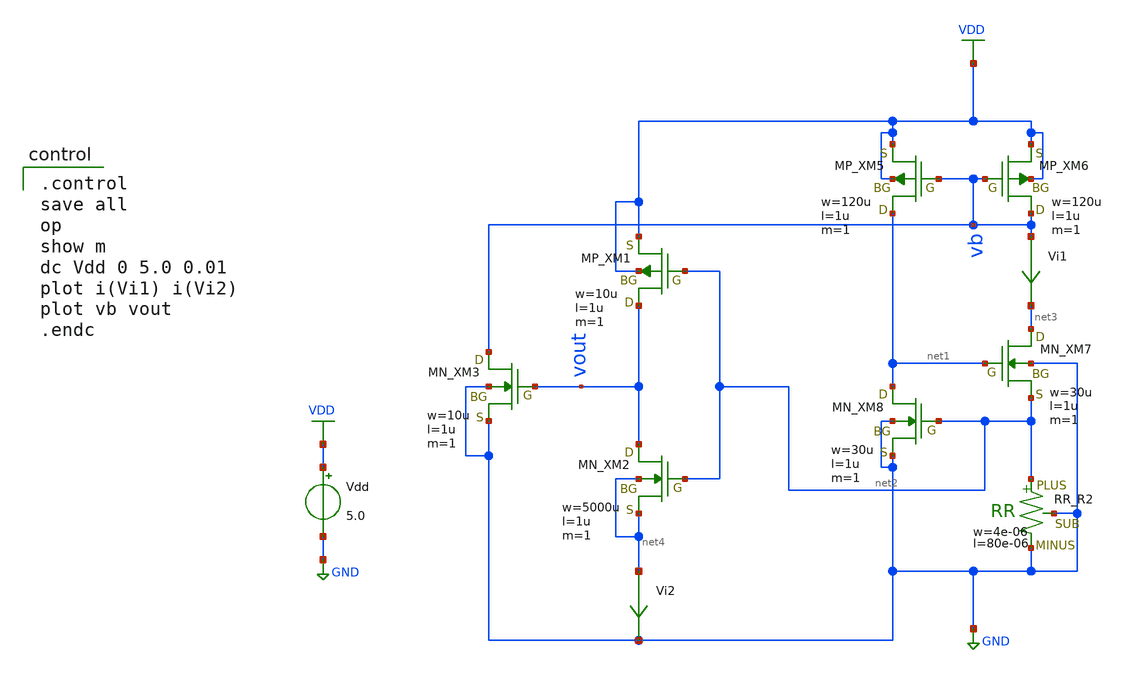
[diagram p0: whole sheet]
** sch_path: schematic/20250924_OSS_Workshop/ishikai/CS/cs_startup_usage_tb.sch
**.subckt cs_startup_usage_tb
Vdd VDD GND 5.0
Vi1 vb net3 0
.save i(vi1)
XM5 net1 vb VDD VDD PMOS w=120u l=1u as=0 ad=0 ps=0 pd=0 nrd=0 nrs=0 m=1
XM6 vb vb VDD VDD PMOS w=120u l=1u as=0 ad=0 ps=0 pd=0 nrd=0 nrs=0 m=1
XM7 net3 net1 net2 GND NMOS w=30u l=1u as=0 ad=0 ps=0 pd=0 nrd=0 nrs=0 m=1
XM8 net1 net2 GND GND NMOS w=30u l=1u as=0 ad=0 ps=0 pd=0 nrd=0 nrs=0 m=1
XR2 net2 GND GND F_RR w=4e-06 R=1 l=80e-06 tc1=0 tc2=0
XM1 vout net2 VDD VDD PMOS w=10u l=1u as=0 ad=0 ps=0 pd=0 nrd=0 nrs=0 m=1
XM2 vout net2 net4 net4 NMOS w=5000u l=1u as=0 ad=0 ps=0 pd=0 nrd=0 nrs=0 m=1
XM3 vb vout GND GND NMOS w=10u l=1u as=0 ad=0 ps=0 pd=0 nrd=0 nrs=0 m=1
Vi2 net4 GND 0
.save i(vi2)
**** begin user architecture code

.control
save all
op
show m
dc Vdd 0 5.0 0.01
plot i(Vi1) i(Vi2)
plot vb vout
.endc

 .include $::LIB/../ip62_models
**** end user architecture code
**.ends
.GLOBAL GND
.GLOBAL VDD
.end
